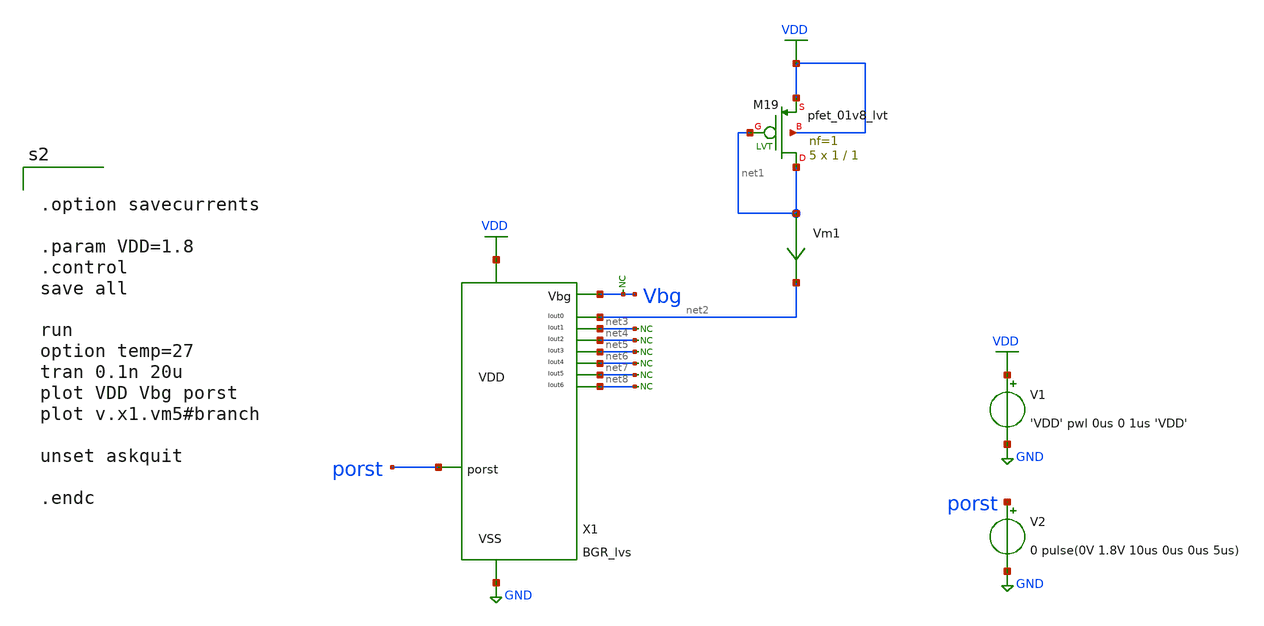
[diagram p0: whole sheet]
** sch_path: xschem/current_reference/tb_BGR_tran_lvs.sch
**.subckt tb_BGR_tran_lvs
V1 VDD GND 'VDD' pwl 0us 0 1us 'VDD'
V2 porst GND 0 pulse(0V 1.8V 10us 0us 0us 5us)
* noconn #net3
* noconn #net4
XM19 net1 net1 VDD VDD sky130_fd_pr__pfet_01v8_lvt L=1 W=1 nf=1 ad='int((nf+1)/2) * W/nf * 0.29' as='int((nf+2)/2) * W/nf * 0.29'
+ pd='2*int((nf+1)/2) * (W/nf + 0.29)' ps='2*int((nf+2)/2) * (W/nf + 0.29)' nrd='0.29 / W' nrs='0.29 / W'
+ sa=0 sb=0 sd=0 mult=5 m=5
Vm1 net1 net2 0
.save i(vm1)
* noconn Vbg
* noconn #net5
* noconn #net6
* noconn #net7
* noconn #net8
X1 porst VDD GND Vbg net2 net3 net4 net5 net6 net7 net8 BGR_lvs
**** begin user architecture code

** opencircuitdesign pdks install
.lib $::SKYWATER_MODELS/sky130.lib.spice tt




.option savecurrents

.param VDD=1.8
.control
save all

run
option temp=27
tran 0.1n 20u
plot VDD Vbg porst
plot v.x1.vm5#branch

unset askquit

.endc


**** end user architecture code
**.ends
.GLOBAL VDD
.GLOBAL GND
.end
